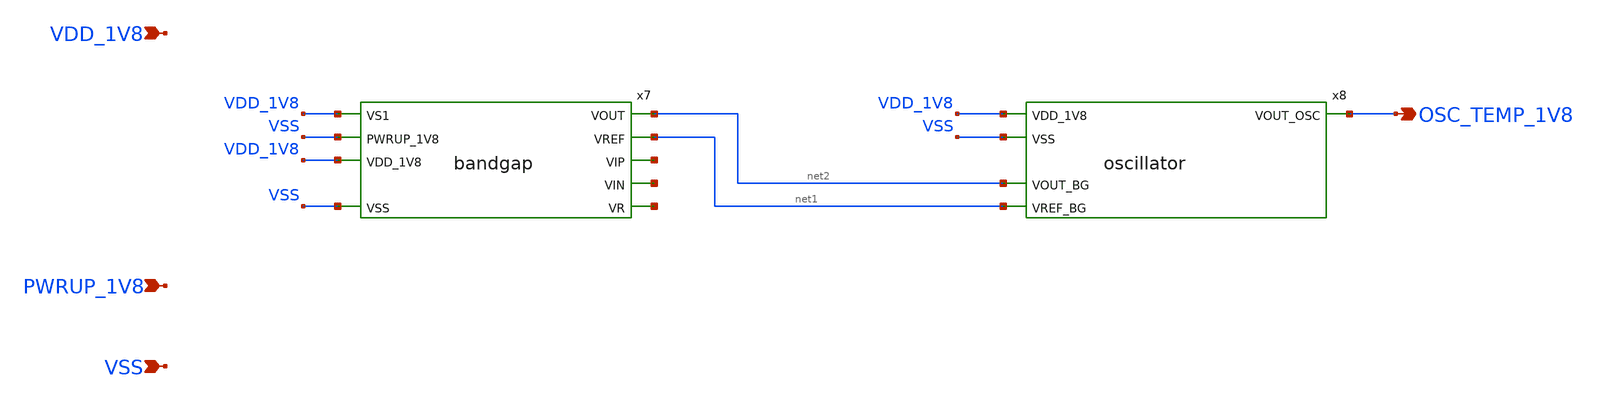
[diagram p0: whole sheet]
** sch_path: design/LELO_GR01_SKY130A/LELO_GR01.sch
**.subckt LELO_GR01 VDD_1V8 VSS PWRUP_1V8 OSC_TEMP_1V8
*.ipin VDD_1V8
*.ipin VSS
*.ipin PWRUP_1V8
*.opin OSC_TEMP_1V8
x7 net2 net1 VDD_1V8 VSS VDD_1V8 net3 net4 VSS net5 bandgap
x8 OSC_TEMP_1V8 VDD_1V8 VSS net2 net1 oscillator
**.ends
.end
